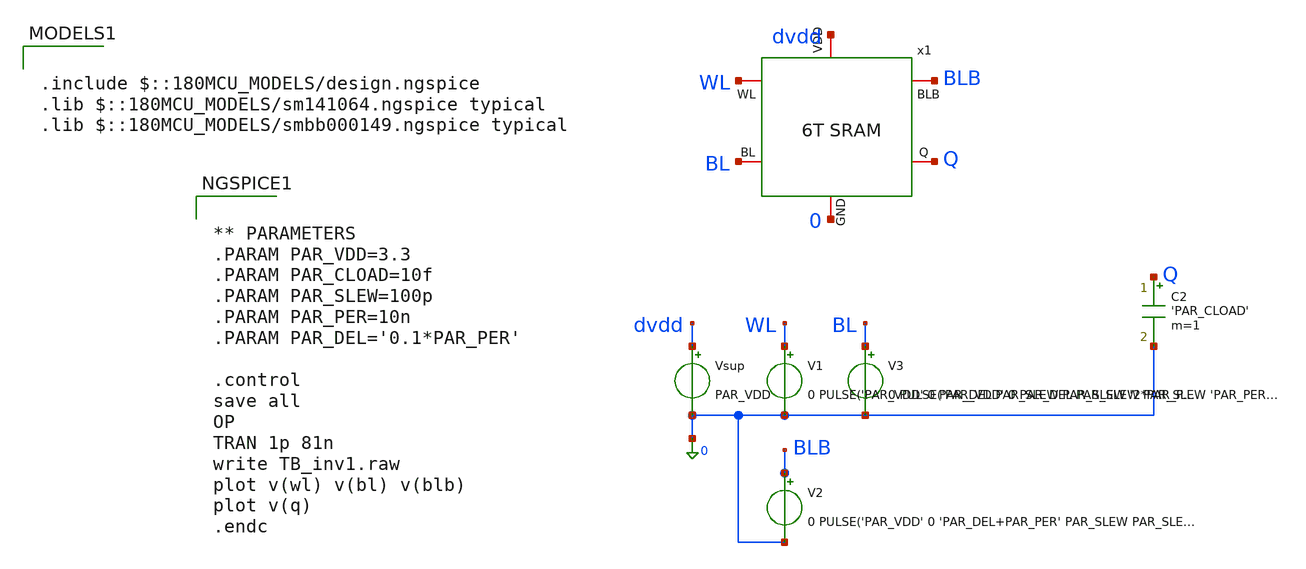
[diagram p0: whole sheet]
** sch_path: src/schematic/6T4BIT/6T4bit_tb.sch
**.subckt 6T4bit_tb
V1 WL 0 0 PULSE('PAR_VDD' 0 PAR_DEL PAR_SLEW PAR_SLEW '2*PAR_PER' '4.0*PAR_PER')
Vsup dvdd 0 PAR_VDD
V2 BLB 0 0 PULSE('PAR_VDD' 0 'PAR_DEL+PAR_PER' PAR_SLEW PAR_SLEW 'PAR_PER' '2.0*PAR_PER')
x1 dvdd WL BLB BL Q 0 6T4bit
C2 Q 0 'PAR_CLOAD' m=1
V3 BL 0 0 PULSE('PAR_VDD' 0 PAR_DEL PAR_SLEW PAR_SLEW 'PAR_PER' '2.0*PAR_PER')
**** begin user architecture code

.include $::180MCU_MODELS/design.ngspice
.lib $::180MCU_MODELS/sm141064.ngspice typical
.lib $::180MCU_MODELS/smbb000149.ngspice typical



** PARAMETERS
.PARAM PAR_VDD=3.3
.PARAM PAR_CLOAD=10f
.PARAM PAR_SLEW=100p
.PARAM PAR_PER=10n
.PARAM PAR_DEL='0.1*PAR_PER'

.control
save all
OP
TRAN 1p 81n
write TB_inv1.raw
plot v(wl) v(bl) v(blb)
plot v(q)
.endc


**** end user architecture code
**.ends

* expanding   symbol:  src/schematic/6T4BIT/6T4bit.sym # of pins=6
** sym_path: src/schematic/6T4BIT/6T4bit.sym
** sch_path: src/schematic/6T4BIT/6T4bit.sch
.subckt 6T4bit VDD WL BLB BL Q GND
*.iopin BLB
*.iopin GND
*.iopin Q
*.iopin VDD
*.iopin BL
*.iopin WL
XSR1_M6 Q WL BL GND nfet_03v3 L=0.28u W=0.22u nf=1 ad='int((nf+1)/2) * W/nf * 0.18u' as='int((nf+2)/2) * W/nf * 0.18u'
+ pd='2*int((nf+1)/2) * (W/nf + 0.18u)' ps='2*int((nf+2)/2) * (W/nf + 0.18u)' nrd='0.18u / W' nrs='0.18u / W'
+ sa=0 sb=0 sd=0 m=1
XSR1_M3 Q net1 Q Q pfet_03v3 L=0.28u W=0.22u nf=1 ad='int((nf+1)/2) * W/nf * 0.18u' as='int((nf+2)/2) * W/nf * 0.18u'
+ pd='2*int((nf+1)/2) * (W/nf + 0.18u)' ps='2*int((nf+2)/2) * (W/nf + 0.18u)' nrd='0.18u / W' nrs='0.18u / W'
+ sa=0 sb=0 sd=0 m=1
XSR1_M4 net1 Q Q Q pfet_03v3 L=0.28u W=0.22u nf=1 ad='int((nf+1)/2) * W/nf * 0.18u' as='int((nf+2)/2) * W/nf * 0.18u'
+ pd='2*int((nf+1)/2) * (W/nf + 0.18u)' ps='2*int((nf+2)/2) * (W/nf + 0.18u)' nrd='0.18u / W' nrs='0.18u / W'
+ sa=0 sb=0 sd=0 m=1
XSR1_M5 BLB WL net1 GND nfet_03v3 L=0.28u W=0.22u nf=1 ad='int((nf+1)/2) * W/nf * 0.18u' as='int((nf+2)/2) * W/nf * 0.18u'
+ pd='2*int((nf+1)/2) * (W/nf + 0.18u)' ps='2*int((nf+2)/2) * (W/nf + 0.18u)' nrd='0.18u / W' nrs='0.18u / W'
+ sa=0 sb=0 sd=0 m=1
XSR1_M1 Q net1 GND GND nfet_03v3 L=0.28u W=0.22u nf=1 ad='int((nf+1)/2) * W/nf * 0.18u' as='int((nf+2)/2) * W/nf * 0.18u'
+ pd='2*int((nf+1)/2) * (W/nf + 0.18u)' ps='2*int((nf+2)/2) * (W/nf + 0.18u)' nrd='0.18u / W' nrs='0.18u / W'
+ sa=0 sb=0 sd=0 m=1
XSR1_M2 net1 Q GND GND nfet_03v3 L=0.28u W=0.22u nf=1 ad='int((nf+1)/2) * W/nf * 0.18u' as='int((nf+2)/2) * W/nf * 0.18u'
+ pd='2*int((nf+1)/2) * (W/nf + 0.18u)' ps='2*int((nf+2)/2) * (W/nf + 0.18u)' nrd='0.18u / W' nrs='0.18u / W'
+ sa=0 sb=0 sd=0 m=1
.ends

.end
